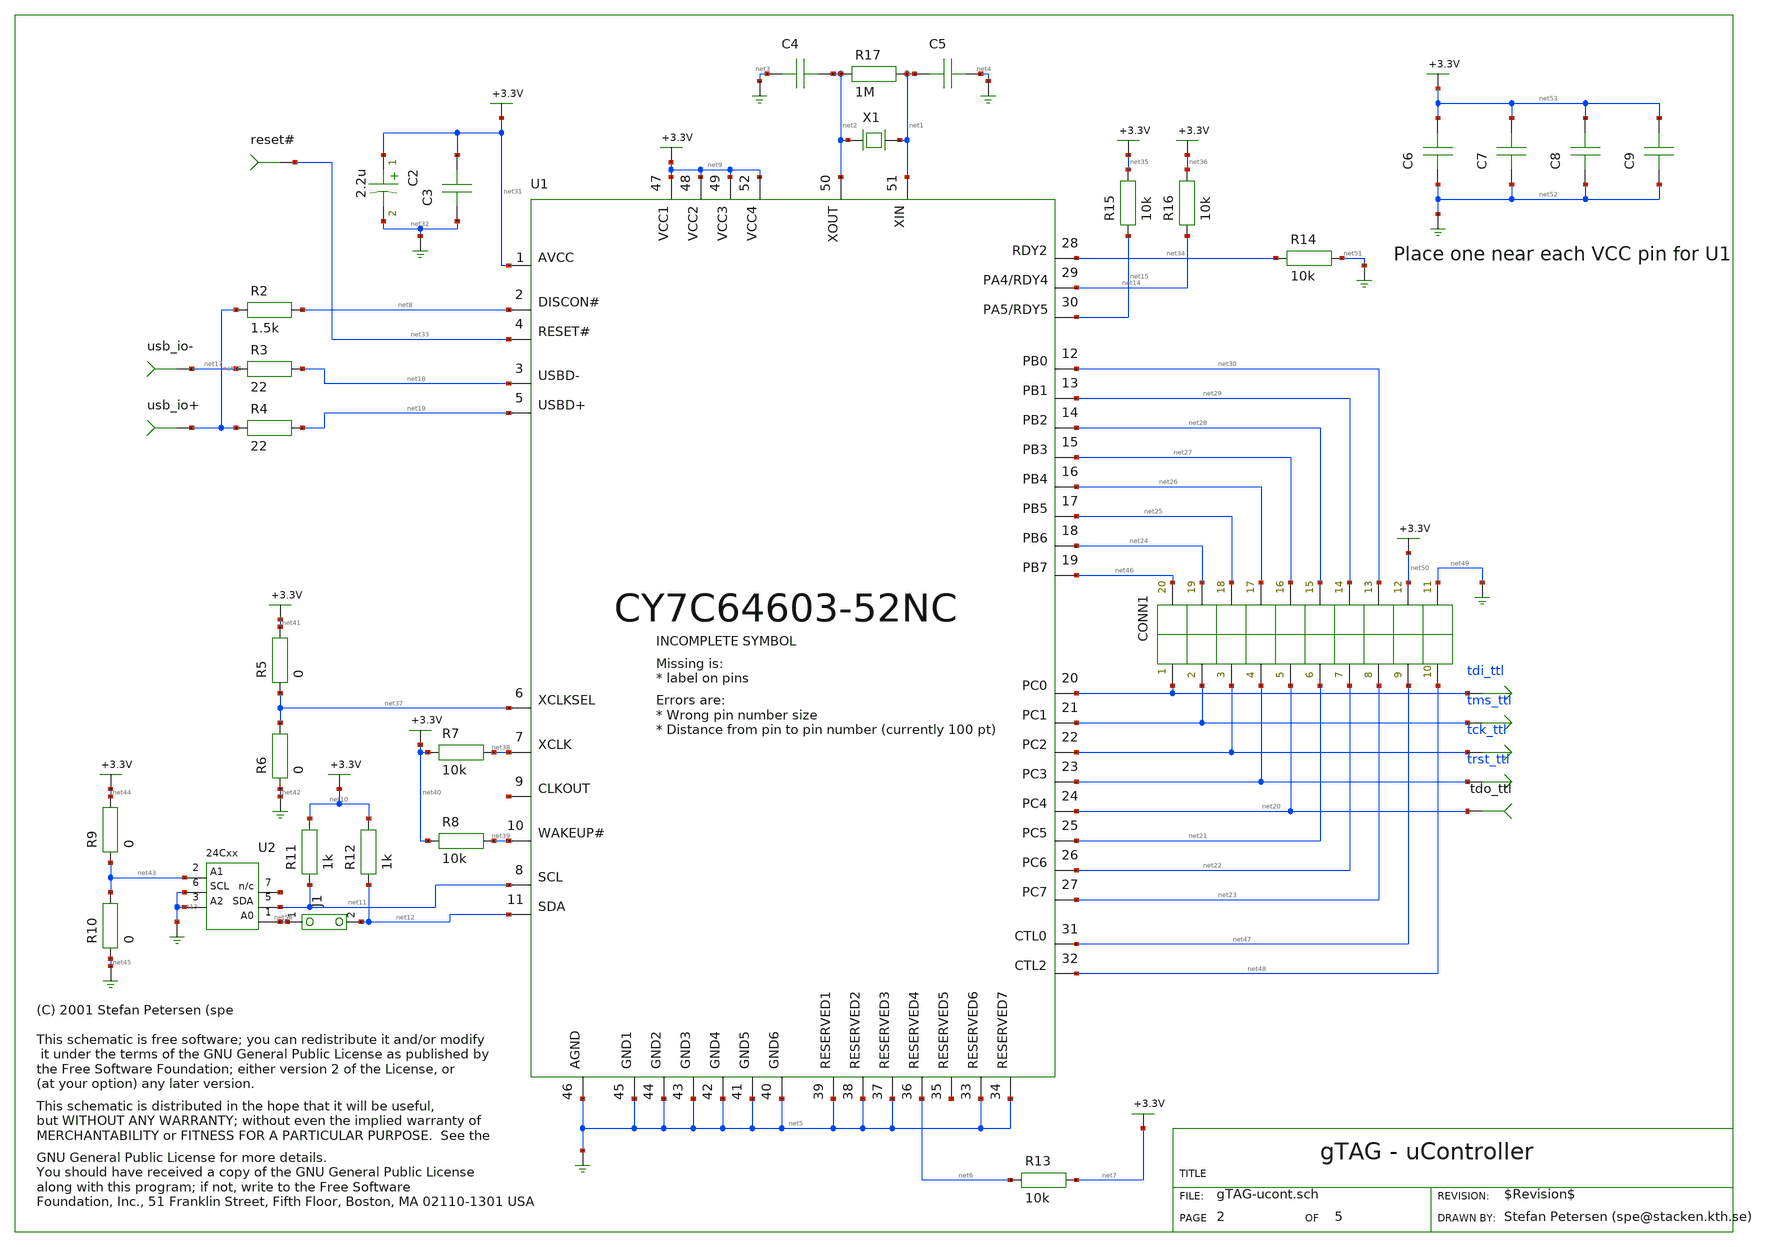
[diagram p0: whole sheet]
** sch_path: xschem_library/gschem_import/gTAG-ucont.sch
* copyleft.sym
**.subckt gTAG-ucont tdi_ttl tms_ttl tck_ttl trst_ttl
U2 net43 net13 net13 net54 net11 net55 Vcc GND
X1 net2 net1 12MHz
R17 net2 net1 1M
C4 net3 net2 30p
C5 net1 net4 30p
R13 net6 net7 10k
usb_io+ net16
usb_io- net17
R2 net16 net8 1.5k
R12 net12 net10 1k
R11 net11 net10 1k
R6 net42 net37 0
R15 net15 net35 10k
R4 net16 net19 22
R3 net17 net18 22
R5 net37 net41 0
R7 net40 net38 10k
R8 net40 net39 10k
C3 net32 net31 100n
C2 net31 net32 2.2u
U1 net9 net11 net12 net39 net31 net1 net2 net5 net5 net14 net15 net56 net5 net9 net5 net37 net5 net8
+ net6 net57 net5 net5 net5 net18 net19 net5 net9 net33 net30 net29 net28 net27 net26 net25 net24 net46
+ net48 net38 net5 net9 net47 net34 tdi_ttl tms_ttl tck_ttl trst_ttl net5 net20 net21 net22 net23 net5
tdo_ttl net20
R16 net14 net36 10k
R14 net34 net51 10k
R10 net45 net43 0
R9 net43 net44 0
C6 net52 net53 100n
C7 net52 net53 100n
C8 net52 net53 100n
C9 net52 net53 100n
C9
J1 net12 net54
reset# net33
CONN1 tdi_ttl tms_ttl tck_ttl trst_ttl net20 net21 net22 net23 net47 net48 net49 net50 net30 net29
+ net28 net27 net26 net25 net24 net46
**.ends
.end
